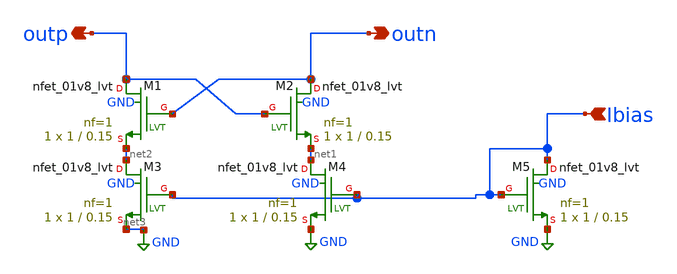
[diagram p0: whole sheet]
** sch_path: generators/lc-dco/xschem_rundir/diff_cross_mirror_verilog.sch
**.subckt diff_cross_mirror_verilog Ibias outn outp
*.ipin Ibias
*.opin outn
*.opin outp
XM1 outp outn net2 GND sky130_fd_pr__nfet_01v8_lvt L=0.15 W=1 nf=1 ad='int((1 + 1)/2) * 1 / 1 * 0.29'
+ as='int((1 + 2)/2) * 1 / 1 * 0.29' pd='2*int((1 + 1)/2) * (1 / 1 + 0.29)' ps='2*int((1 + 2)/2) * (1 / 1 + 0.29)'
+ nrd='0.29 / 1 ' nrs='0.29 / 1 ' sa=0 sb=0 sd=0 mult=1 m=1
XM2 outn outp net1 GND sky130_fd_pr__nfet_01v8_lvt L=0.15 W=1 nf=1 ad='int((1 + 1)/2) * 1 / 1 * 0.29'
+ as='int((1 + 2)/2) * 1 / 1 * 0.29' pd='2*int((1 + 1)/2) * (1 / 1 + 0.29)' ps='2*int((1 + 2)/2) * (1 / 1 + 0.29)'
+ nrd='0.29 / 1 ' nrs='0.29 / 1 ' sa=0 sb=0 sd=0 mult=1 m=1
XM4 net1 Ibias GND GND sky130_fd_pr__nfet_01v8_lvt L=0.15 W=1 nf=1 ad='int((1 + 1)/2) * 1 / 1 * 0.29'
+ as='int((1 + 2)/2) * 1 / 1 * 0.29' pd='2*int((1 + 1)/2) * (1 / 1 + 0.29)' ps='2*int((1 + 2)/2) * (1 / 1 + 0.29)'
+ nrd='0.29 / 1 ' nrs='0.29 / 1 ' sa=0 sb=0 sd=0 mult=1 m=1
XM5 Ibias Ibias GND GND sky130_fd_pr__nfet_01v8_lvt L=0.15 W=1 nf=1 ad='int((1 + 1)/2) * 1 / 1 * 0.29'
+ as='int((1 + 2)/2) * 1 / 1 * 0.29' pd='2*int((1 + 1)/2) * (1 / 1 + 0.29)' ps='2*int((1 + 2)/2) * (1 / 1 + 0.29)'
+ nrd='0.29 / 1 ' nrs='0.29 / 1 ' sa=0 sb=0 sd=0 mult=1 m=1
XM3 net2 Ibias net3 GND sky130_fd_pr__nfet_01v8_lvt L=0.15 W=1 nf=1 ad='int((1 + 1)/2) * 1 / 1 * 0.29'
+ as='int((1 + 2)/2) * 1 / 1 * 0.29' pd='2*int((1 + 1)/2) * (1 / 1 + 0.29)' ps='2*int((1 + 2)/2) * (1 / 1 + 0.29)'
+ nrd='0.29 / 1 ' nrs='0.29 / 1 ' sa=0 sb=0 sd=0 mult=1 m=1
**.ends
.GLOBAL GND
.end
